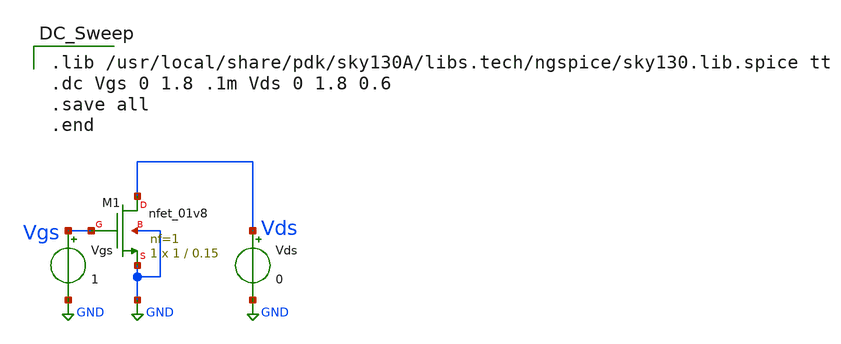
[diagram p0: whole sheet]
** sch_path: MOS/NMOS/Schematic/nmos.sch
**.subckt nmos
XM1 Vds Vgs GND GND sky130_fd_pr__nfet_01v8 L=0.15 W=1 nf=1 ad='int((nf+1)/2) * W/nf * 0.29' as='int((nf+2)/2) * W/nf * 0.29'
+ pd='2*int((nf+1)/2) * (W/nf + 0.29)' ps='2*int((nf+2)/2) * (W/nf + 0.29)' nrd='0.29 / W' nrs='0.29 / W'
+ sa=0 sb=0 sd=0 mult=1 m=1
Vgs Vgs GND 1
Vds Vds GND 0
**** begin user architecture code

.lib /usr/local/share/pdk/sky130A/libs.tech/ngspice/sky130.lib.spice tt
.dc Vgs 0 1.8 .1m Vds 0 1.8 0.6
.save all
.end

**** end user architecture code
**.ends
.GLOBAL GND
.end
